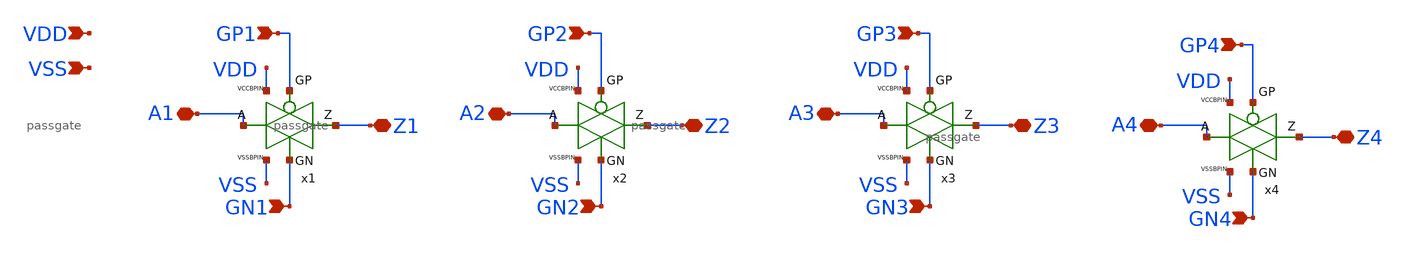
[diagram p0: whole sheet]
** sch_path: xschem/passgatex4.sch
**.subckt passgatex4 VDD VSS GP1 GN1 A1 Z1 GP2 GN2 A2 Z2 GP3 GN3 A3 Z3 GP4 GN4 A4 Z4
*.ipin VDD
*.ipin VSS
*.ipin GP1
*.ipin GN1
*.iopin A1
*.iopin Z1
*.ipin GP2
*.ipin GN2
*.iopin A2
*.iopin Z2
*.ipin GP3
*.ipin GN3
*.iopin A3
*.iopin Z3
*.ipin GP4
*.ipin GN4
*.iopin A4
*.iopin Z4
x1 Z1 A1 GP1 GN1 VSS VDD passgate
x2 Z2 A2 GP2 GN2 VSS VDD passgate
x3 Z3 A3 GP3 GN3 VSS VDD passgate
x4 Z4 A4 GP4 GN4 VSS VDD passgate
**.ends

* expanding   symbol:  /home/ttuser/tt08-wowa2/xschem/passgate.sym # of pins=6
** sym_path: xschem/passgate.sym
** sch_path: xschem/passgate.sch
.subckt passgate Z A GP GN VSSBPIN VCCBPIN
*.ipin GN
*.ipin VCCBPIN
*.ipin VSSBPIN
*.ipin GP
*.iopin A
*.iopin Z
XM1 Z GN A VSSBPIN sky130_fd_pr__nfet_01v8_lvt L=0.35 W=8 nf=1 ad='int((nf+1)/2) * W/nf * 0.29' as='int((nf+2)/2) * W/nf * 0.29'
+ pd='2*int((nf+1)/2) * (W/nf + 0.29)' ps='2*int((nf+2)/2) * (W/nf + 0.29)' nrd='0.29 / W' nrs='0.29 / W'
+ sa=0 sb=0 sd=0 mult=2 m=2
XM3 Z GP A VCCBPIN sky130_fd_pr__pfet_01v8_lvt L=0.35 W=10 nf=1 ad='int((nf+1)/2) * W/nf * 0.29' as='int((nf+2)/2) * W/nf * 0.29'
+ pd='2*int((nf+1)/2) * (W/nf + 0.29)' ps='2*int((nf+2)/2) * (W/nf + 0.29)' nrd='0.29 / W' nrs='0.29 / W'
+ sa=0 sb=0 sd=0 mult=2 m=2
.ends

.end
